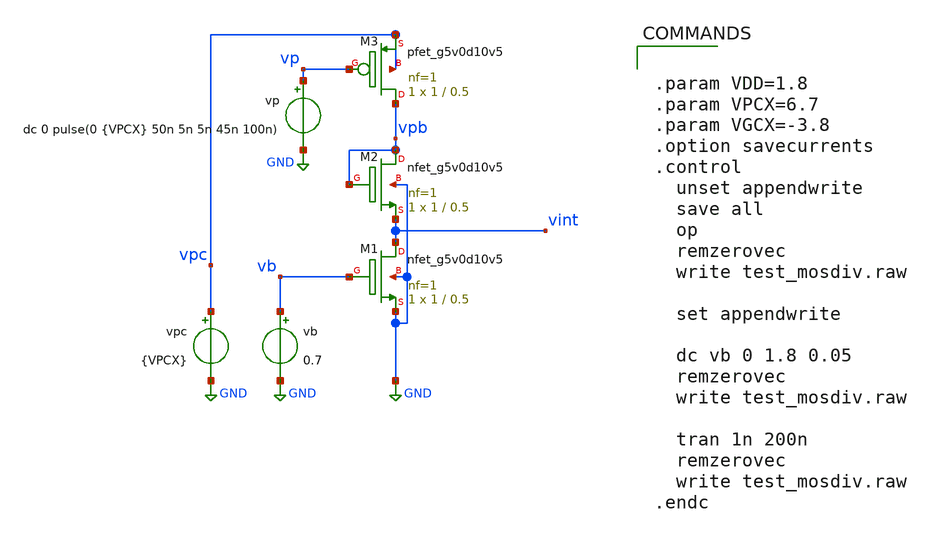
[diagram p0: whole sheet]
** sch_path: row_drivers/test_mosdiv.sch
**.subckt test_mosdiv
vb vb GND 0.7
XM1 vint vb GND GND sky130_fd_pr__nfet_g5v0d10v5 L=0.5 W=1 nf=1 ad='int((nf+1)/2) * W/nf * 0.29' as='int((nf+2)/2) * W/nf * 0.29'
+ pd='2*int((nf+1)/2) * (W/nf + 0.29)' ps='2*int((nf+2)/2) * (W/nf + 0.29)' nrd='0.29 / W' nrs='0.29 / W'
+ sa=0 sb=0 sd=0 mult=1 m=1
XM2 vpb vpb vint GND sky130_fd_pr__nfet_g5v0d10v5 L=0.5 W=1 nf=1 ad='int((nf+1)/2) * W/nf * 0.29' as='int((nf+2)/2) * W/nf * 0.29'
+ pd='2*int((nf+1)/2) * (W/nf + 0.29)' ps='2*int((nf+2)/2) * (W/nf + 0.29)' nrd='0.29 / W' nrs='0.29 / W'
+ sa=0 sb=0 sd=0 mult=1 m=1
vpc vpc GND {VPCX}
XM3 vpb vp vpc vpc sky130_fd_pr__pfet_g5v0d10v5 L=0.5 W=1 nf=1 ad='int((nf+1)/2) * W/nf * 0.29' as='int((nf+2)/2) * W/nf * 0.29'
+ pd='2*int((nf+1)/2) * (W/nf + 0.29)' ps='2*int((nf+2)/2) * (W/nf + 0.29)' nrd='0.29 / W' nrs='0.29 / W'
+ sa=0 sb=0 sd=0 mult=1 m=1
vp vp GND dc 0 pulse(0 {VPCX} 50n 5n 5n 45n 100n)
**** begin user architecture code

** opencircuitdesign pdks install
.lib $::SKYWATER_MODELS/sky130.lib.spice tt




.param VDD=1.8
.param VPCX=6.7
.param VGCX=-3.8
.option savecurrents
.control
  unset appendwrite
  save all
  op
  remzerovec
  write test_mosdiv.raw

  set appendwrite

  dc vb 0 1.8 0.05
  remzerovec
  write test_mosdiv.raw

  tran 1n 200n
  remzerovec
  write test_mosdiv.raw
.endc


**** end user architecture code
**.ends
.GLOBAL GND
.end
